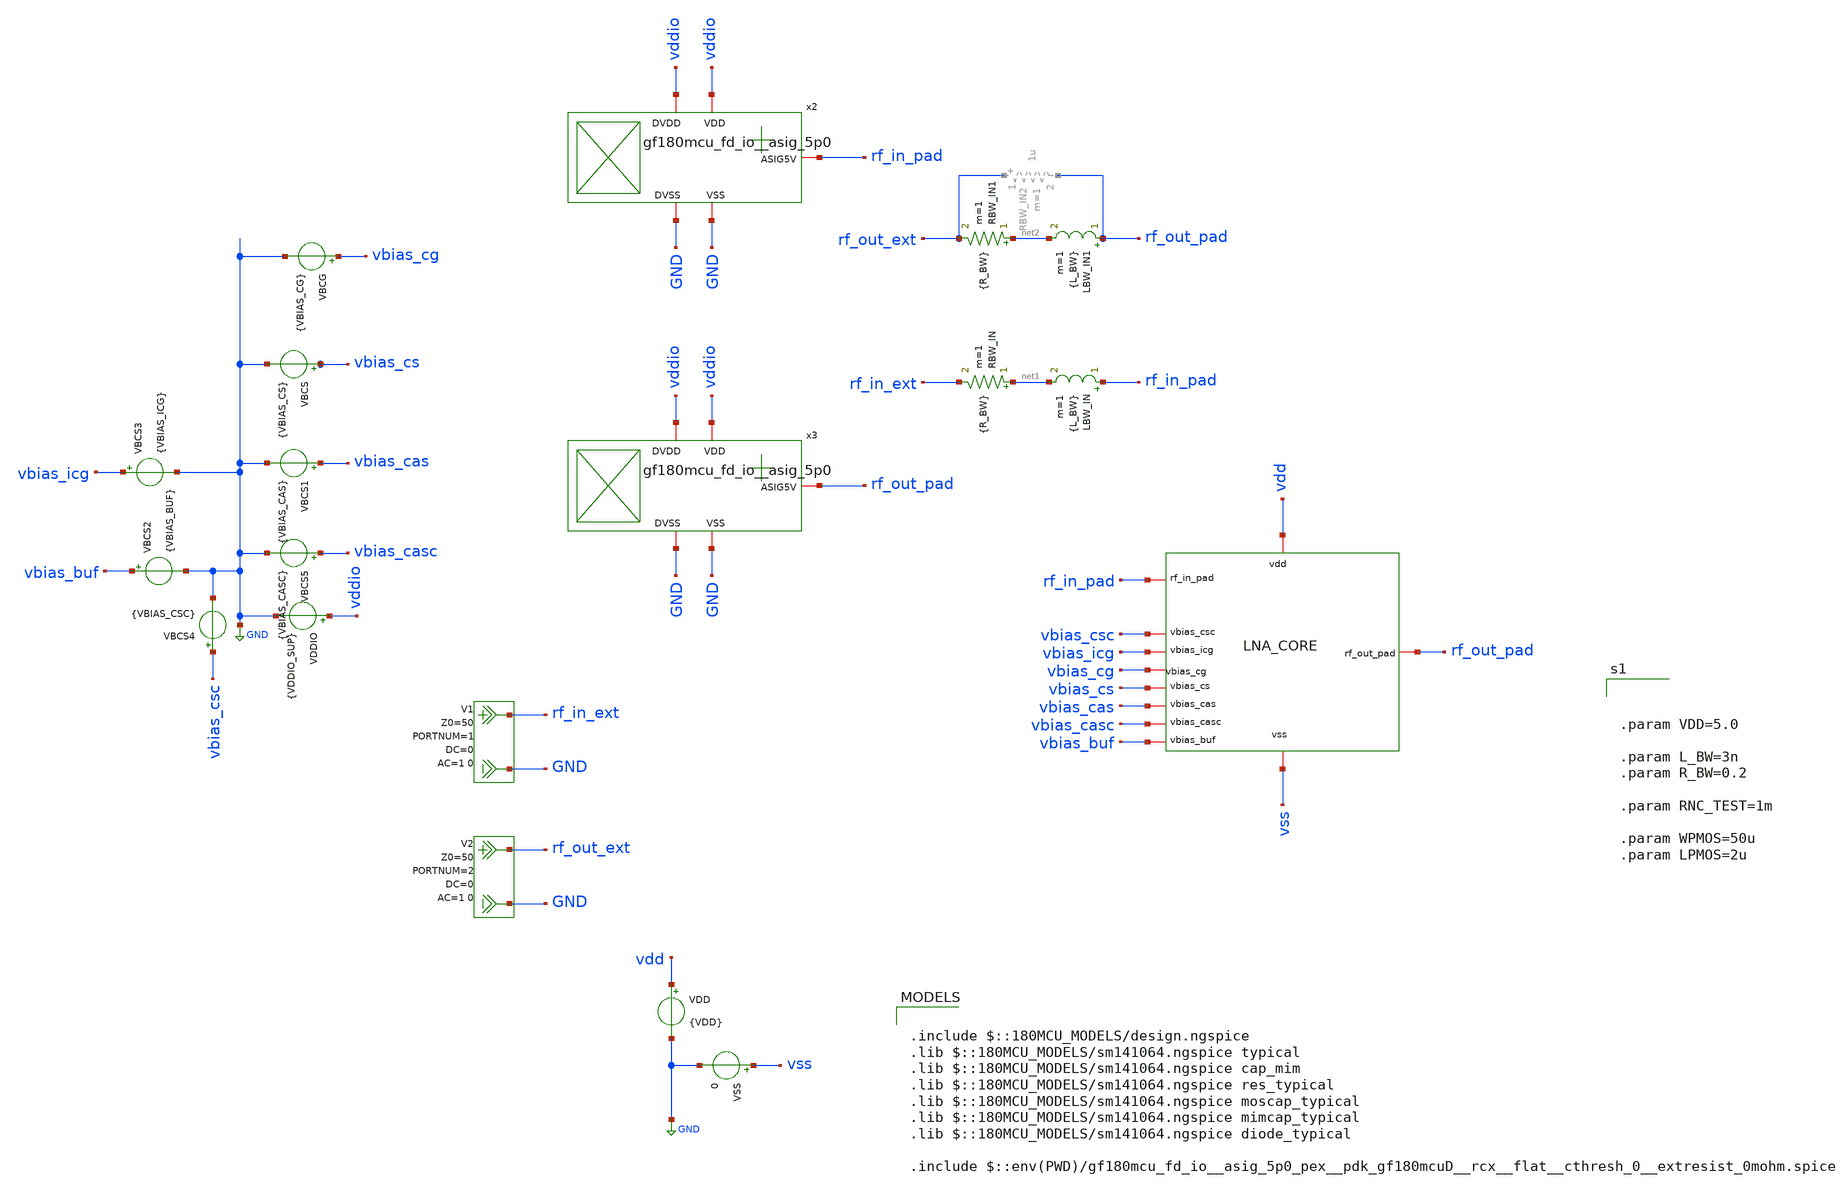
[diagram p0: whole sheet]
** sch_path: xschem/lna-core_tb.sch
**.subckt lna-core_tb
x1 vbias_cg rf_in_pad vbias_cs rf_out_pad vdd vbias_cas vss vbias_casc vbias_buf vbias_icg vbias_csc
+ lna_core
VDD vdd GND {VDD}
VSS vss GND 0
LBW_IN rf_in_pad net1 {L_BW} m=1
RBW_IN net1 rf_in_ext {R_BW} m=1
LBW_IN1 rf_out_pad net2 {L_BW} m=1
RBW_IN1 net2 rf_out_ext {R_BW} m=1
VBCG vbias_cg GND {VBIAS_CG}
VDDIO vddio GND {VDDIO_SUP}
VBCS vbias_cs GND {VBIAS_CS}
VBCS1 vbias_cas GND {VBIAS_CAS}
VBCS2 vbias_buf GND {VBIAS_BUF}
VBCS3 vbias_icg GND {VBIAS_ICG}
VBCS4 vbias_csc GND {VBIAS_CSC}
VBCS5 vbias_casc GND {VBIAS_CASC}
V1 rf_in_ext GND DC 0 AC 1 0 portnum 1 z0 50
V2 rf_out_ext GND DC 0 AC 1 0 portnum 2 z0 50
x2 rf_in_pad vddio GND vddio GND gf180mcu_fd_io__asig_5p0
x3 rf_out_pad vddio GND vddio GND gf180mcu_fd_io__asig_5p0
**** begin user architecture code

.include $::180MCU_MODELS/design.ngspice
.lib $::180MCU_MODELS/sm141064.ngspice typical
.lib $::180MCU_MODELS/sm141064.ngspice cap_mim
.lib $::180MCU_MODELS/sm141064.ngspice res_typical
.lib $::180MCU_MODELS/sm141064.ngspice moscap_typical
.lib $::180MCU_MODELS/sm141064.ngspice mimcap_typical
.lib $::180MCU_MODELS/sm141064.ngspice diode_typical

.include $::env(PWD)/gf180mcu_fd_io__asig_5p0_pex__pdk_gf180mcuD__rcx__flat__cthresh_0__extresist_0mohm.spice




.param VDD=5.0

.param L_BW=3n
.param R_BW=0.2

.param RNC_TEST=1m

.param WPMOS=50u
.param LPMOS=2u






.control

set noaskquit
set wr_singlescale
set wr_vecnames
set numdgt=10

let target_gain_bw=10.0

echo ============================================================ > lna_core_06V_cgcs_report.txt
echo GF180MCU_LNA_CORE_06V_CGCS_DETAILED_REPORT >> lna_core_06V_cgcs_report.txt
echo TARGET_FREQUENCY_HZ 2.400e9 >> lna_core_06V_cgcs_report.txt
echo TARGET_BAND_HZ 2.300e9 2.500e9 >> lna_core_06V_cgcs_report.txt
echo GAIN_BANDWIDTH_THRESHOLD_DB 10.0 >> lna_core_06V_cgcs_report.txt
echo PORT_REFERENCE_OHM 50 >> lna_core_06V_cgcs_report.txt
echo NOTE_HIERARCHY LNA_CORE_INSTANCE_IS_X1 >> lna_core_06V_cgcs_report.txt
echo ============================================================ >> lna_core_06V_cgcs_report.txt

* =============================================================================
* DC OPERATING POINT
* =============================================================================

op

* Top-level supply and bias values (real pins of this circuit only:
* vbias_cg, vbias_cs, vbias_cas -- vbias_casc/buf/icg/csc are unused
* dangling ports left over on the lna_core symbol).
let pdcop=1e3*abs(i(VDD))*v(vdd)
let icoreop=abs(i(VDD))

let v_vddop=v(vdd)
let v_vbias_cgop=v(vbias_cg)
let v_vbias_csop=v(vbias_cs)
let v_vbias_casop=v(vbias_cas)

* LNA internal nodes are inside instance x1.
let vnet1op=v(x1.net1)
let vm2op=v(x1.vm2)
let vnet2op=v(x1.net2)
let vm1op=v(x1.vm1)
let vxop=v(x1.vx)
let vgcsop=v(x1.g_cs)
let vgcgop=v(x1.g_cg)

* XM2: CG input device, source-degenerated by L1/Rs + Leq/RLeq (fed-back common-gate, no tail
*+ source).
let id2op=abs(@m.x1.xm2.m0[id])
let gm2op=@m.x1.xm2.m0[gm]
let gmb2op=@m.x1.xm2.m0[gmbs]
let gds2op=@m.x1.xm2.m0[gds]
let vgs2op=@m.x1.xm2.m0[vgs]
let vds2op=@m.x1.xm2.m0[vds]
let vbs2op=@m.x1.xm2.m0[vbs]
let vth2op=@m.x1.xm2.m0[vth]
let vov2op=vgs2op-vth2op
let vdsat2op=abs(@m.x1.xm2.m0[vdsat])
let sat2op=vds2op-vdsat2op
let gmid2op=gm2op/(id2op+1e-30)
let ro2op=1/(gds2op+1e-30)

* XM1: CS gain device.
let id1op=abs(@m.x1.xm1.m0[id])
let gm1op=@m.x1.xm1.m0[gm]
let gmb1op=@m.x1.xm1.m0[gmbs]
let gds1op=@m.x1.xm1.m0[gds]
let vgs1op=@m.x1.xm1.m0[vgs]
let vds1op=@m.x1.xm1.m0[vds]
let vbs1op=@m.x1.xm1.m0[vbs]
let vth1op=@m.x1.xm1.m0[vth]
let vov1op=vgs1op-vth1op
let vdsat1op=abs(@m.x1.xm1.m0[vdsat])
let sat1op=vds1op-vdsat1op
let gmid1op=gm1op/(id1op+1e-30)
let ro1op=1/(gds1op+1e-30)

* XM4: cascode on top of XM1, gate fixed at vbias_cas.
let id4op=abs(@m.x1.xm4.m0[id])
let gm4op=@m.x1.xm4.m0[gm]
let gmb4op=@m.x1.xm4.m0[gmbs]
let gds4op=@m.x1.xm4.m0[gds]
let vgs4op=@m.x1.xm4.m0[vgs]
let vds4op=@m.x1.xm4.m0[vds]
let vbs4op=@m.x1.xm4.m0[vbs]
let vth4op=@m.x1.xm4.m0[vth]
let vov4op=vgs4op-vth4op
let vdsat4op=abs(@m.x1.xm4.m0[vdsat])
let sat4op=vds4op-vdsat4op
let gmid4op=gm4op/(id4op+1e-30)
let ro4op=1/(gds4op+1e-30)

set op_pdc=$&pdcop
set op_icore=$&icoreop
set op_vdd=$&v_vddop
set op_vbias_cg=$&v_vbias_cgop
set op_vbias_cs=$&v_vbias_csop
set op_vbias_cas=$&v_vbias_casop

set op_vnet1=$&vnet1op
set op_vm2=$&vm2op
set op_vnet2=$&vnet2op
set op_vm1=$&vm1op
set op_vx=$&vxop
set op_vgcs=$&vgcsop
set op_vgcg=$&vgcgop

set op_id1=$&id1op
set op_gm1=$&gm1op
set op_gmb1=$&gmb1op
set op_gds1=$&gds1op
set op_vgs1=$&vgs1op
set op_vds1=$&vds1op
set op_vbs1=$&vbs1op
set op_vth1=$&vth1op
set op_vov1=$&vov1op
set op_vdsat1=$&vdsat1op
set op_sat1=$&sat1op
set op_gmid1=$&gmid1op
set op_ro1=$&ro1op

set op_id2=$&id2op
set op_gm2=$&gm2op
set op_gmb2=$&gmb2op
set op_gds2=$&gds2op
set op_vgs2=$&vgs2op
set op_vds2=$&vds2op
set op_vbs2=$&vbs2op
set op_vth2=$&vth2op
set op_vov2=$&vov2op
set op_vdsat2=$&vdsat2op
set op_sat2=$&sat2op
set op_gmid2=$&gmid2op
set op_ro2=$&ro2op

set op_id4=$&id4op
set op_gm4=$&gm4op
set op_gmb4=$&gmb4op
set op_gds4=$&gds4op
set op_vgs4=$&vgs4op
set op_vds4=$&vds4op
set op_vbs4=$&vbs4op
set op_vth4=$&vth4op
set op_vov4=$&vov4op
set op_vdsat4=$&vdsat4op
set op_sat4=$&sat4op
set op_gmid4=$&gmid4op
set op_ro4=$&ro4op

echo ============================================================ >> lna_core_06V_cgcs_report.txt
echo DC_SUPPLY_AND_BIAS >> lna_core_06V_cgcs_report.txt
echo PDC_mW $op_pdc ICORE_A $op_icore >> lna_core_06V_cgcs_report.txt
echo BIAS_V VDD $op_vdd VBIAS_CG $op_vbias_cg VBIAS_CS $op_vbias_cs VBIAS_CAS $op_vbias_cas >>
+ lna_core_06V_cgcs_report.txt
echo ============================================================ >> lna_core_06V_cgcs_report.txt
echo DC_LNA_INTERNAL_NODE_VOLTAGES >> lna_core_06V_cgcs_report.txt
echo NODES_V NET1 $op_vnet1 VM2 $op_vm2 NET2 $op_vnet2 VM1 $op_vm1 VX $op_vx G_CS $op_vgcs G_CG
+ $op_vgcg >> lna_core_06V_cgcs_report.txt
echo ============================================================ >> lna_core_06V_cgcs_report.txt
echo TRANSISTOR_OPERATING_POINTS >> lna_core_06V_cgcs_report.txt
echo FIELDS ID_A GM_S GMBS_S GDS_S VGS_V VDS_V VBS_V VTH_V VOV_V VDSAT_V SAT_MARGIN_V
+ GM_OVER_ID_1_PER_V RO_OHM >> lna_core_06V_cgcs_report.txt
echo XM2_CG_FEDBACK ID $op_id2 GM $op_gm2 GMBS $op_gmb2 GDS $op_gds2 VGS $op_vgs2 VDS $op_vds2 VBS
+ $op_vbs2 VTH $op_vth2 VOV $op_vov2 VDSAT $op_vdsat2 SAT_MARGIN $op_sat2 GMID $op_gmid2 RO $op_ro2 >>
+ lna_core_06V_cgcs_report.txt
echo XM1_CS ID $op_id1 GM $op_gm1 GMBS $op_gmb1 GDS $op_gds1 VGS $op_vgs1 VDS $op_vds1 VBS $op_vbs1
+ VTH $op_vth1 VOV $op_vov1 VDSAT $op_vdsat1 SAT_MARGIN $op_sat1 GMID $op_gmid1 RO $op_ro1 >>
+ lna_core_06V_cgcs_report.txt
echo XM4_CS_CASCODE ID $op_id4 GM $op_gm4 GMBS $op_gmb4 GDS $op_gds4 VGS $op_vgs4 VDS $op_vds4 VBS
+ $op_vbs4 VTH $op_vth4 VOV $op_vov4 VDSAT $op_vdsat4 SAT_MARGIN $op_sat4 GMID $op_gmid4 RO $op_ro4 >>
+ lna_core_06V_cgcs_report.txt

destroy $curplot

* =============================================================================
* SINGLE BROADBAND RF ANALYSIS
* One reset and one SP run are used for all 1 MHz to 7 GHz RF results.
* Target-band values are extracted from the same dataset.
* =============================================================================

reset
sp lin 7000 1Meg 7Gig 1
set rfplot=$curplot

let fghz=frequency/1e9

let s11db=db(s_1_1)
let s21db=db(s_2_1)
let s12db=db(s_1_2)
let s22db=db(s_2_2)

let s11re=real(s_1_1)
let s11im=imag(s_1_1)
let s21re=real(s_2_1)
let s21im=imag(s_2_1)
let s12re=real(s_1_2)
let s12im=imag(s_1_2)
let s22re=real(s_2_2)
let s22im=imag(s_2_2)

let z22re=real(z_2_2)
let z22im=imag(z_2_2)

let nfdb=real(NF)
let nfmin_db=real(NFmin)

let delta=s_1_1*s_2_2-s_1_2*s_2_1
let delta_mag=mag(delta)
let a11=mag(s_1_1)
let a12=mag(s_1_2)
let a21=mag(s_2_1)
let a22=mag(s_2_2)
let mu=(1-a11*a11)/(mag(s_2_2-delta*conj(s_1_1))+mag(s_1_2*s_2_1))
let mup=(1-a22*a22)/(mag(s_1_1-delta*conj(s_2_2))+mag(s_1_2*s_2_1))
let kval=(1-a11*a11-a22*a22+delta_mag*delta_mag)/(2*a12*a21)

let zin=50*(1+s_1_1)/(1-s_1_1)
let zout=50*(1+s_2_2)/(1-s_2_2)
let zin_re=real(zin)
let zin_im=imag(zin)
let zout_re=real(zout)
let zout_im=imag(zout)

let npts=length(frequency)

let ilo=0
let icenter=0
let ihi=0
let errlo=abs(frequency[0]-2.3e9)
let errcenter=abs(frequency[0]-2.4e9)
let errhi=abs(frequency[0]-2.5e9)
let ii=1

while ii < npts
let newerr=abs(frequency[ii]-2.3e9)
if newerr < errlo
let errlo=newerr
let ilo=ii
end
let newerr=abs(frequency[ii]-2.4e9)
if newerr < errcenter
let errcenter=newerr
let icenter=ii
end
let newerr=abs(frequency[ii]-2.5e9)
if newerr < errhi
let errhi=newerr
let ihi=ii
end
let ii=ii+1
end

let center_freq=frequency[icenter]
let s11c=s11db[icenter]
let s21c=s21db[icenter]
let s12c=s12db[icenter]
let s22c=s22db[icenter]
let s11rc=s11re[icenter]
let s11ic=s11im[icenter]
let s21rc=s21re[icenter]
let s21ic=s21im[icenter]
let s12rc=s12re[icenter]
let s12ic=s12im[icenter]
let s22rc=s22re[icenter]
let s22ic=s22im[icenter]
let nfc=nfdb[icenter]
let nfminc=nfmin_db[icenter]
let muc=mu[icenter]
let mupc=mup[icenter]
let kc=kval[icenter]
let dmc=delta_mag[icenter]
let zinrc=zin_re[icenter]
let zinic=zin_im[icenter]
let zoutrc=zout_re[icenter]
let zoutic=zout_im[icenter]

let s11min=s11db[ilo]
let s11max=s11db[ilo]
let s21min=s21db[ilo]
let s21max=s21db[ilo]
let s12min=s12db[ilo]
let s12max=s12db[ilo]
let s22min=s22db[ilo]
let s22max=s22db[ilo]
let nfbandmin=nfdb[ilo]
let nfbandmax=nfdb[ilo]
let nfminbandmin=nfmin_db[ilo]
let nfminbandmax=nfmin_db[ilo]
let mumin=mu[ilo]
let mupmin=mup[ilo]
let kmin=kval[ilo]
let dmax=delta_mag[ilo]

let s11min_i=ilo
let s11max_i=ilo
let s21min_i=ilo
let s21max_i=ilo
let s12min_i=ilo
let s12max_i=ilo
let s22min_i=ilo
let s22max_i=ilo
let nfmin_i=ilo
let nfmax_i=ilo
let nfminpar_min_i=ilo
let nfminpar_max_i=ilo
let mumin_i=ilo
let mupmin_i=ilo
let kmin_i=ilo
let dmax_i=ilo

let ii=ilo
while ii <= ihi
if s11db[ii] < s11min
let s11min=s11db[ii]
let s11min_i=ii
end
if s11db[ii] > s11max
let s11max=s11db[ii]
let s11max_i=ii
end
if s21db[ii] < s21min
let s21min=s21db[ii]
let s21min_i=ii
end
if s21db[ii] > s21max
let s21max=s21db[ii]
let s21max_i=ii
end
if s12db[ii] < s12min
let s12min=s12db[ii]
let s12min_i=ii
end
if s12db[ii] > s12max
let s12max=s12db[ii]
let s12max_i=ii
end
if s22db[ii] < s22min
let s22min=s22db[ii]
let s22min_i=ii
end
if s22db[ii] > s22max
let s22max=s22db[ii]
let s22max_i=ii
end
if nfdb[ii] < nfbandmin
let nfbandmin=nfdb[ii]
let nfmin_i=ii
end
if nfdb[ii] > nfbandmax
let nfbandmax=nfdb[ii]
let nfmax_i=ii
end
if nfmin_db[ii] < nfminbandmin
let nfminbandmin=nfmin_db[ii]
let nfminpar_min_i=ii
end
if nfmin_db[ii] > nfminbandmax
let nfminbandmax=nfmin_db[ii]
let nfminpar_max_i=ii
end
if mu[ii] < mumin
let mumin=mu[ii]
let mumin_i=ii
end
if mup[ii] < mupmin
let mupmin=mup[ii]
let mupmin_i=ii
end
if kval[ii] < kmin
let kmin=kval[ii]
let kmin_i=ii
end
if delta_mag[ii] > dmax
let dmax=delta_mag[ii]
let dmax_i=ii
end
let ii=ii+1
end

let gain_ripple=s21max-s21min

let s11min_f=frequency[s11min_i]
let s11max_f=frequency[s11max_i]
let s21min_f=frequency[s21min_i]
let s21max_f=frequency[s21max_i]
let s12min_f=frequency[s12min_i]
let s12max_f=frequency[s12max_i]
let s22min_f=frequency[s22min_i]
let s22max_f=frequency[s22max_i]
let nfmin_f=frequency[nfmin_i]
let nfmax_f=frequency[nfmax_i]
let nfminpar_min_f=frequency[nfminpar_min_i]
let nfminpar_max_f=frequency[nfminpar_max_i]
let mumin_f=frequency[mumin_i]
let mupmin_f=frequency[mupmin_i]
let kmin_f=frequency[kmin_i]
let dmax_f=frequency[dmax_i]

let imax=0
let gainmax=s21db[0]
let ii=1
while ii < npts
if s21db[ii] > gainmax
let gainmax=s21db[ii]
let imax=ii
end
let ii=ii+1
end
let peakfreq=frequency[imax]

echo ============================================================ >> lna_core_06V_cgcs_report.txt
echo RF_AT_2P400_GHZ_FROM_SINGLE_BROADBAND_SWEEP >> lna_core_06V_cgcs_report.txt
echo ACTUAL_SAMPLE_HZ $&center_freq >> lna_core_06V_cgcs_report.txt
echo S11_DB $&s11c REAL $&s11rc IMAG $&s11ic >> lna_core_06V_cgcs_report.txt
echo S21_DB $&s21c REAL $&s21rc IMAG $&s21ic >> lna_core_06V_cgcs_report.txt
echo S12_DB $&s12c REAL $&s12rc IMAG $&s12ic >> lna_core_06V_cgcs_report.txt
echo S22_DB $&s22c REAL $&s22rc IMAG $&s22ic >> lna_core_06V_cgcs_report.txt
echo NF_DB $&nfc NFMIN_DB $&nfminc >> lna_core_06V_cgcs_report.txt
echo MU $&muc MUP $&mupc K $&kc DELTA_MAG $&dmc >> lna_core_06V_cgcs_report.txt
echo ZIN_OHM RE $&zinrc IM $&zinic >> lna_core_06V_cgcs_report.txt
echo ZOUT_OHM RE $&zoutrc IM $&zoutic >> lna_core_06V_cgcs_report.txt

echo ============================================================ >> lna_core_06V_cgcs_report.txt
echo RF_MIN_MAX_FROM_2P300_TO_2P500_GHZ >> lna_core_06V_cgcs_report.txt
echo S11_MIN_DB $&s11min AT_HZ $&s11min_f S11_MAX_DB $&s11max AT_HZ $&s11max_f >>
+ lna_core_06V_cgcs_report.txt
echo S21_MIN_DB $&s21min AT_HZ $&s21min_f S21_MAX_DB $&s21max AT_HZ $&s21max_f GAIN_RIPPLE_DB
+ $&gain_ripple >> lna_core_06V_cgcs_report.txt
echo S12_MIN_DB $&s12min AT_HZ $&s12min_f S12_MAX_DB $&s12max AT_HZ $&s12max_f >>
+ lna_core_06V_cgcs_report.txt
echo S22_MIN_DB $&s22min AT_HZ $&s22min_f S22_MAX_DB $&s22max AT_HZ $&s22max_f >>
+ lna_core_06V_cgcs_report.txt
echo NF_MIN_DB $&nfbandmin AT_HZ $&nfmin_f NF_MAX_DB $&nfbandmax AT_HZ $&nfmax_f >>
+ lna_core_06V_cgcs_report.txt
echo NFMIN_PARAMETER_MIN_DB $&nfminbandmin AT_HZ $&nfminpar_min_f NFMIN_PARAMETER_MAX_DB
+ $&nfminbandmax AT_HZ $&nfminpar_max_f >> lna_core_06V_cgcs_report.txt
echo MU_MIN $&mumin AT_HZ $&mumin_f MUP_MIN $&mupmin AT_HZ $&mupmin_f >>
+ lna_core_06V_cgcs_report.txt
echo K_MIN $&kmin AT_HZ $&kmin_f DELTA_MAX $&dmax AT_HZ $&dmax_f >> lna_core_06V_cgcs_report.txt

echo ============================================================ >> lna_core_06V_cgcs_report.txt
echo BROADBAND_GAIN_CHECK_1MHZ_TO_7GHZ >> lna_core_06V_cgcs_report.txt
echo GAIN_AT_2P4_DB $&s21c >> lna_core_06V_cgcs_report.txt
echo BROADBAND_PEAK_HZ $&peakfreq PEAK_GAIN_DB $&gainmax >> lna_core_06V_cgcs_report.txt

echo ============================================================ >> lna_core_06V_cgcs_report.txt
echo TARGET_CENTERED_S21_GE_10DB_BAND >> lna_core_06V_cgcs_report.txt
if s21c >= 10.0
let bwlo=icenter
let bwhi=icenter
let search=1
while search = 1
if bwlo > 0
if s21db[bwlo-1] >= 10.0
let bwlo=bwlo-1
else
let search=0
end
else
let search=0
end
end
let search=1
while search = 1
if bwhi < npts-1
if s21db[bwhi+1] >= 10.0
let bwhi=bwhi+1
else
let search=0
end
else
let search=0
end
end
let bwflo=frequency[bwlo]
let bwfhi=frequency[bwhi]
let bwval=bwfhi-bwflo
let bwcenter=0.5*(bwfhi+bwflo)
let bwfbw=100*bwval/(bwcenter+1e-30)
echo LOWER_HZ $&bwflo UPPER_HZ $&bwfhi BANDWIDTH_HZ $&bwval BAND_CENTER_HZ $&bwcenter
+ FRACTIONAL_BW_PERCENT $&bwfbw >> lna_core_06V_cgcs_report.txt
else
echo NO_VALID_TARGET_CENTERED_BAND S21_AT_2P4_DB $&s21c >> lna_core_06V_cgcs_report.txt
end

echo ============================================================ >> lna_core_06V_cgcs_report.txt
echo GLOBAL_CONTIGUOUS_S21_GE_10DB_BAND_AROUND_PEAK >> lna_core_06V_cgcs_report.txt
if gainmax >= 10.0
let bwlo=imax
let bwhi=imax
let search=1
while search = 1
if bwlo > 0
if s21db[bwlo-1] >= 10.0
let bwlo=bwlo-1
else
let search=0
end
else
let search=0
end
end
let search=1
while search = 1
if bwhi < npts-1
if s21db[bwhi+1] >= 10.0
let bwhi=bwhi+1
else
let search=0
end
else
let search=0
end
end
let bwflo=frequency[bwlo]
let bwfhi=frequency[bwhi]
let bwval=bwfhi-bwflo
let bwcenter=0.5*(bwfhi+bwflo)
let bwfbw=100*bwval/(bwcenter+1e-30)
echo LOWER_HZ $&bwflo UPPER_HZ $&bwfhi BANDWIDTH_HZ $&bwval BAND_CENTER_HZ $&bwcenter
+ FRACTIONAL_BW_PERCENT $&bwfbw >> lna_core_06V_cgcs_report.txt
else
echo NO_S21_ABOVE_10DB_FROM_1MHZ_TO_7GHZ PEAK_GAIN_DB $&gainmax PEAK_FREQUENCY_HZ $&peakfreq >>
+ lna_core_06V_cgcs_report.txt
end

wrdata lna_core_06V_cgcs_target_band.dat frequency s_1_1 s_2_1 s_1_2 s_2_2 s11db s21db s12db s22db
+ nfdb nfmin_db kval mu mup delta_mag zin_re zin_im zout_re zout_im
wrdata lna_core_06V_cgcs_broadband.dat frequency s11db s21db s12db s22db nfdb nfmin_db kval mu mup
+ delta_mag zin_re zin_im zout_re zout_im

reset

* =============================================================================
* WIDEBAND STABILITY 10 MHZ TO 30 GHZ
* =============================================================================

sp dec 101 10Meg 30G 1
set stabilityplot=$curplot

let wbdelta=s_1_1*s_2_2-s_1_2*s_2_1
let wbmd=mag(wbdelta)
let wba11=mag(s_1_1)
let wba12=mag(s_1_2)
let wba21=mag(s_2_1)
let wba22=mag(s_2_2)
let wbmu=(1-wba11*wba11)/(mag(s_2_2-wbdelta*conj(s_1_1))+mag(s_1_2*s_2_1))
let wbmup=(1-wba22*wba22)/(mag(s_1_1-wbdelta*conj(s_2_2))+mag(s_1_2*s_2_1))
let wbk=(1-wba11*wba11-wba22*wba22+wbmd*wbmd)/(2*wba12*wba21)

let wbkmin=minimum(wbk)
let wbmumin=minimum(wbmu)
let wbmupmin=minimum(wbmup)
let wbdmax=maximum(wbmd)

set final_wbkmin=$&wbkmin
set final_wbmumin=$&wbmumin
set final_wbmupmin=$&wbmupmin
set final_wbdmax=$&wbdmax

echo ============================================================ >> lna_core_06V_cgcs_report.txt
echo WIDEBAND_STABILITY_10MHZ_TO_30GHZ >> lna_core_06V_cgcs_report.txt
echo K_MIN $final_wbkmin MU_MIN $final_wbmumin MUP_MIN $final_wbmupmin DELTA_MAX $final_wbdmax >>
+ lna_core_06V_cgcs_report.txt

wrdata lna_core_06V_cgcs_stability.dat frequency wbk wbmu wbmup wbmd

let wbfghz=frequency/1e9

echo ============================================================ >> lna_core_06V_cgcs_report.txt
echo OUTPUT_FILES >> lna_core_06V_cgcs_report.txt
echo REPORT lna_core_06V_cgcs_report.txt >> lna_core_06V_cgcs_report.txt
echo TARGET_DATA lna_core_06V_cgcs_target_band.dat >> lna_core_06V_cgcs_report.txt
echo BROADBAND_DATA lna_core_06V_cgcs_broadband.dat >> lna_core_06V_cgcs_report.txt
echo STABILITY_DATA lna_core_06V_cgcs_stability.dat >> lna_core_06V_cgcs_report.txt
echo PLOTS S_PARAMETERS NF_NFMIN STABILITY_MU_MUP >> lna_core_06V_cgcs_report.txt
echo ============================================================ >> lna_core_06V_cgcs_report.txt

* =============================================================================
* VISIBLE PLOTS
* =============================================================================

setplot $rfplot
setscale fghz

*plot s11db xlimit 2.3 2.5
*plot s21db xlimit 2.3 2.5
*plot s12db xlimit 2.3 2.5
*plot s22db xlimit 2.3 2.5
*plot nfdb nfmin_db xlimit 2.3 2.5

plot s11db s22db s21db xlimit 0.5 5 ylimit -30 30
plot s22re s22im xlimit 2.2 2.6 ylimit -1 1
*plot z22re z22im xlimit 0.5 5
*plot s21db xlimit 0 7
*plot s12db xlimit 0 7
*plot s22db xlimit 0 7
plot nfdb nfmin_db xlimit 0.5 5 ylimit 0 5

setplot $stabilityplot
setscale wbfghz

plot wbmu wbmup xlimit 0.01 30 ylimit 0 3 xlabel 'Frequency (GHz)' ylabel 'Stability factor'

.endc




.param VBIAS_CAS_CG=3.30



.param VDS=5.0
.param VDDIO_SUP=5.0


.param VBIAS_CG=1.00
.param VBIAS_CS=1.20

.param VBIAS_CAS=3.70
.param VBIAS_ICG=1.90
.param VBIAS_BUF=1.30

.param VBIAS_CSC=0.90


.param VBIAS_CASC=3.20
.param RNC_TEST=1m



**** end user architecture code
**.ends
.GLOBAL GND
.end
